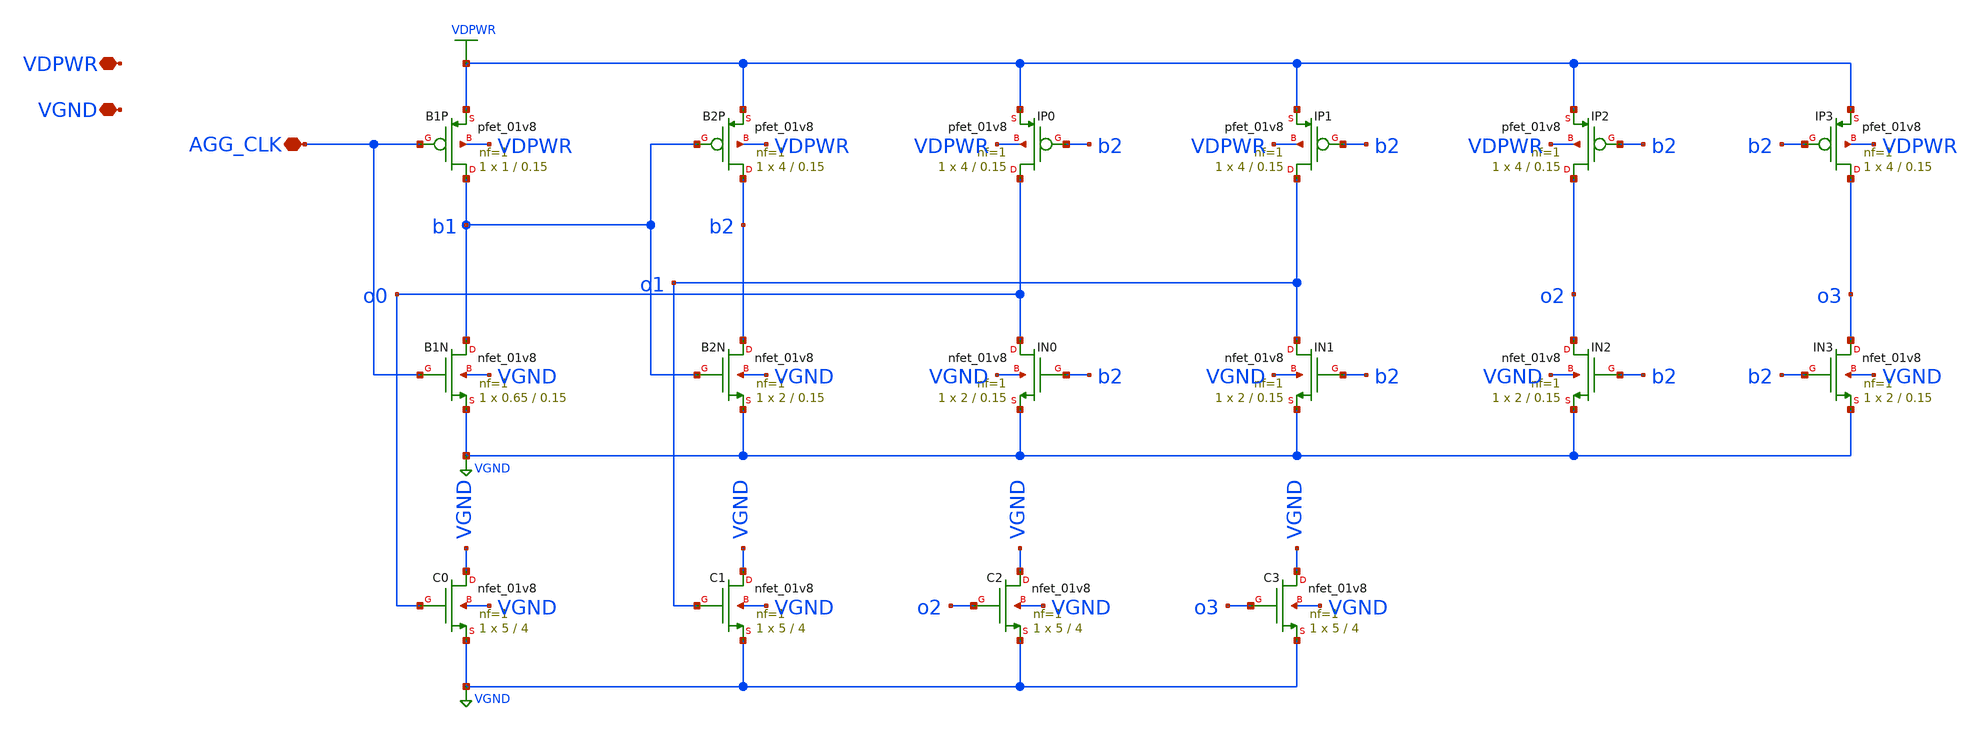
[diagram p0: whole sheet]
** sch_path: cells/ELAD1_AGGRESSOR/schematic/ELAD1_AGGRESSOR.sch
**.subckt ELAD1_AGGRESSOR AGG_CLK VDPWR VGND
*.iopin AGG_CLK
*.iopin VDPWR
*.iopin VGND
XB1N b1 AGG_CLK VGND VGND sky130_fd_pr__nfet_01v8 L=0.15 W=0.65 nf=1 ad='int((1 + 1)/2) * 0.65 / 1 * 0.29'
+ as='int((1 + 2)/2) * 0.65 / 1 * 0.29' pd='2*int((1 + 1)/2) * (0.65 / 1 + 0.29)' ps='2*int((1 + 2)/2) * (0.65 / 1 + 0.29)'
+ nrd='0.29 / 0.65 ' nrs='0.29 / 0.65 ' sa=0 sb=0 sd=0 mult=1 m=1
XB1P b1 AGG_CLK VDPWR VDPWR sky130_fd_pr__pfet_01v8 L=0.15 W=1 nf=1 ad='int((nf+1)/2) * W/nf * 0.29'
+ as='int((nf+2)/2) * W/nf * 0.29' pd='2*int((nf+1)/2) * (W/nf + 0.29)' ps='2*int((nf+2)/2) * (W/nf + 0.29)'
+ nrd='0.29 / W' nrs='0.29 / W' sa=0 sb=0 sd=0 mult=1 m=1
XB2N b2 b1 VGND VGND sky130_fd_pr__nfet_01v8 L=0.15 W=2 nf=1 ad='int((1 + 1)/2) * 2 / 1 * 0.29' as='int((1 + 2)/2) * 2 / 1 * 0.29'
+ pd='2*int((1 + 1)/2) * (2 / 1 + 0.29)' ps='2*int((1 + 2)/2) * (2 / 1 + 0.29)' nrd='0.29 / 2 ' nrs='0.29 / 2 '
+ sa=0 sb=0 sd=0 mult=1 m=1
XB2P b2 b1 VDPWR VDPWR sky130_fd_pr__pfet_01v8 L=0.15 W=4 nf=1 ad='int((nf+1)/2) * W/nf * 0.29' as='int((nf+2)/2) * W/nf * 0.29'
+ pd='2*int((nf+1)/2) * (W/nf + 0.29)' ps='2*int((nf+2)/2) * (W/nf + 0.29)' nrd='0.29 / W' nrs='0.29 / W'
+ sa=0 sb=0 sd=0 mult=1 m=1
XIN0 o0 b2 VGND VGND sky130_fd_pr__nfet_01v8 L=0.15 W=2 nf=1 ad='int((1 + 1)/2) * 2 / 1 * 0.29' as='int((1 + 2)/2) * 2 / 1 * 0.29'
+ pd='2*int((1 + 1)/2) * (2 / 1 + 0.29)' ps='2*int((1 + 2)/2) * (2 / 1 + 0.29)' nrd='0.29 / 2 ' nrs='0.29 / 2 '
+ sa=0 sb=0 sd=0 mult=1 m=1
XIP0 o0 b2 VDPWR VDPWR sky130_fd_pr__pfet_01v8 L=0.15 W=4 nf=1 ad='int((nf+1)/2) * W/nf * 0.29' as='int((nf+2)/2) * W/nf * 0.29'
+ pd='2*int((nf+1)/2) * (W/nf + 0.29)' ps='2*int((nf+2)/2) * (W/nf + 0.29)' nrd='0.29 / W' nrs='0.29 / W'
+ sa=0 sb=0 sd=0 mult=1 m=1
XC0 VGND o0 VGND VGND sky130_fd_pr__nfet_01v8 L=4 W=5 nf=1 ad='int((1 + 1)/2) * 5 / 1 * 0.29' as='int((1 + 2)/2) * 5 / 1 * 0.29'
+ pd='2*int((1 + 1)/2) * (5 / 1 + 0.29)' ps='2*int((1 + 2)/2) * (5 / 1 + 0.29)' nrd='0.29 / 5 ' nrs='0.29 / 5 '
+ sa=0 sb=0 sd=0 mult=1 m=1
XIN1 o1 b2 VGND VGND sky130_fd_pr__nfet_01v8 L=0.15 W=2 nf=1 ad='int((1 + 1)/2) * 2 / 1 * 0.29' as='int((1 + 2)/2) * 2 / 1 * 0.29'
+ pd='2*int((1 + 1)/2) * (2 / 1 + 0.29)' ps='2*int((1 + 2)/2) * (2 / 1 + 0.29)' nrd='0.29 / 2 ' nrs='0.29 / 2 '
+ sa=0 sb=0 sd=0 mult=1 m=1
XIP1 o1 b2 VDPWR VDPWR sky130_fd_pr__pfet_01v8 L=0.15 W=4 nf=1 ad='int((nf+1)/2) * W/nf * 0.29' as='int((nf+2)/2) * W/nf * 0.29'
+ pd='2*int((nf+1)/2) * (W/nf + 0.29)' ps='2*int((nf+2)/2) * (W/nf + 0.29)' nrd='0.29 / W' nrs='0.29 / W'
+ sa=0 sb=0 sd=0 mult=1 m=1
XC1 VGND o1 VGND VGND sky130_fd_pr__nfet_01v8 L=4 W=5 nf=1 ad='int((1 + 1)/2) * 5 / 1 * 0.29' as='int((1 + 2)/2) * 5 / 1 * 0.29'
+ pd='2*int((1 + 1)/2) * (5 / 1 + 0.29)' ps='2*int((1 + 2)/2) * (5 / 1 + 0.29)' nrd='0.29 / 5 ' nrs='0.29 / 5 '
+ sa=0 sb=0 sd=0 mult=1 m=1
XIN2 o2 b2 VGND VGND sky130_fd_pr__nfet_01v8 L=0.15 W=2 nf=1 ad='int((1 + 1)/2) * 2 / 1 * 0.29' as='int((1 + 2)/2) * 2 / 1 * 0.29'
+ pd='2*int((1 + 1)/2) * (2 / 1 + 0.29)' ps='2*int((1 + 2)/2) * (2 / 1 + 0.29)' nrd='0.29 / 2 ' nrs='0.29 / 2 '
+ sa=0 sb=0 sd=0 mult=1 m=1
XIP2 o2 b2 VDPWR VDPWR sky130_fd_pr__pfet_01v8 L=0.15 W=4 nf=1 ad='int((nf+1)/2) * W/nf * 0.29' as='int((nf+2)/2) * W/nf * 0.29'
+ pd='2*int((nf+1)/2) * (W/nf + 0.29)' ps='2*int((nf+2)/2) * (W/nf + 0.29)' nrd='0.29 / W' nrs='0.29 / W'
+ sa=0 sb=0 sd=0 mult=1 m=1
XC2 VGND o2 VGND VGND sky130_fd_pr__nfet_01v8 L=4 W=5 nf=1 ad='int((1 + 1)/2) * 5 / 1 * 0.29' as='int((1 + 2)/2) * 5 / 1 * 0.29'
+ pd='2*int((1 + 1)/2) * (5 / 1 + 0.29)' ps='2*int((1 + 2)/2) * (5 / 1 + 0.29)' nrd='0.29 / 5 ' nrs='0.29 / 5 '
+ sa=0 sb=0 sd=0 mult=1 m=1
XIN3 o3 b2 VGND VGND sky130_fd_pr__nfet_01v8 L=0.15 W=2 nf=1 ad='int((1 + 1)/2) * 2 / 1 * 0.29' as='int((1 + 2)/2) * 2 / 1 * 0.29'
+ pd='2*int((1 + 1)/2) * (2 / 1 + 0.29)' ps='2*int((1 + 2)/2) * (2 / 1 + 0.29)' nrd='0.29 / 2 ' nrs='0.29 / 2 '
+ sa=0 sb=0 sd=0 mult=1 m=1
XIP3 o3 b2 VDPWR VDPWR sky130_fd_pr__pfet_01v8 L=0.15 W=4 nf=1 ad='int((nf+1)/2) * W/nf * 0.29' as='int((nf+2)/2) * W/nf * 0.29'
+ pd='2*int((nf+1)/2) * (W/nf + 0.29)' ps='2*int((nf+2)/2) * (W/nf + 0.29)' nrd='0.29 / W' nrs='0.29 / W'
+ sa=0 sb=0 sd=0 mult=1 m=1
XC3 VGND o3 VGND VGND sky130_fd_pr__nfet_01v8 L=4 W=5 nf=1 ad='int((1 + 1)/2) * 5 / 1 * 0.29' as='int((1 + 2)/2) * 5 / 1 * 0.29'
+ pd='2*int((1 + 1)/2) * (5 / 1 + 0.29)' ps='2*int((1 + 2)/2) * (5 / 1 + 0.29)' nrd='0.29 / 5 ' nrs='0.29 / 5 '
+ sa=0 sb=0 sd=0 mult=1 m=1
**.ends
.GLOBAL VGND
.GLOBAL VDPWR
.end
